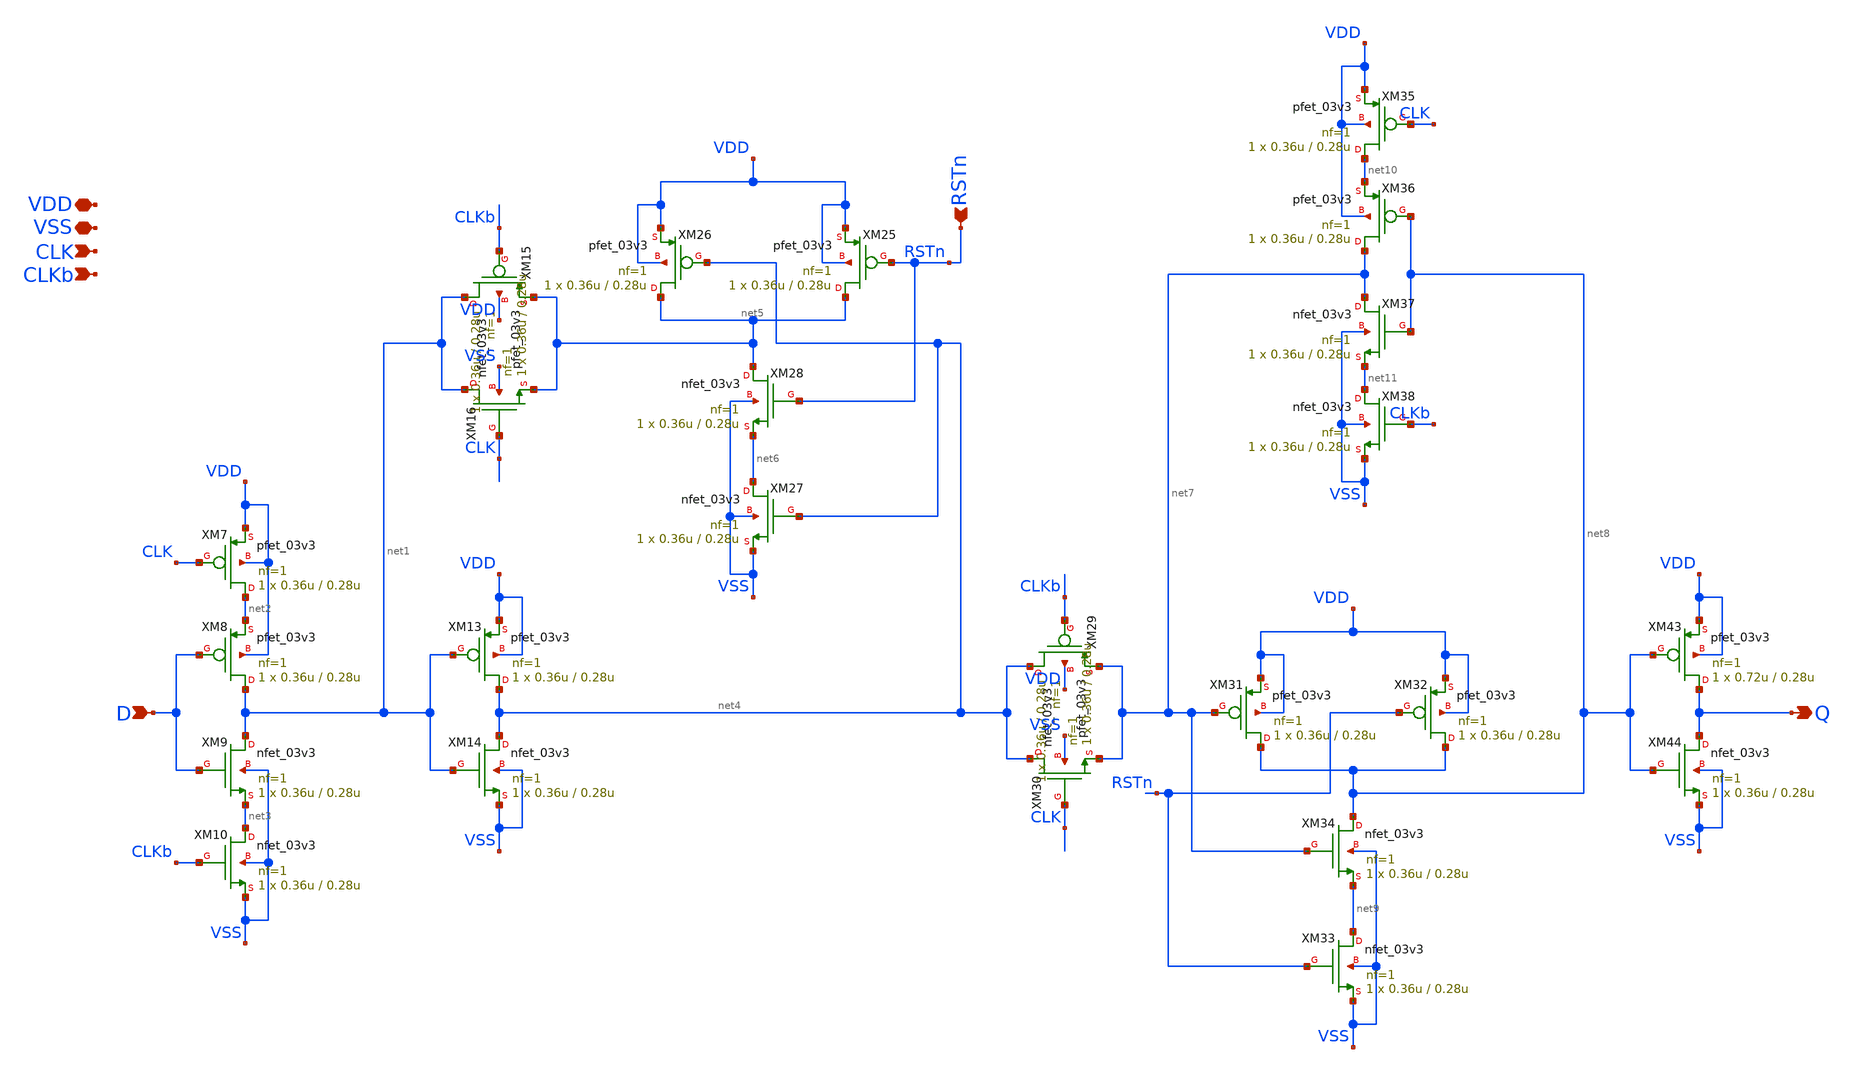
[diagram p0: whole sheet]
** sch_path: CAD6/dff.sch
**.subckt dff D Q RSTn CLK CLKb VDD VSS
*.ipin D
*.opin Q
*.ipin RSTn
*.ipin CLK
*.ipin CLKb
*.iopin VDD
*.iopin VSS
XM7 net2 CLK VDD VDD pfet_03v3 L=0.28u W=0.36u nf=1 ad='int((nf+1)/2) * W/nf * 0.18u' as='int((nf+2)/2) * W/nf * 0.18u'
+ pd='2*int((nf+1)/2) * (W/nf + 0.18u)' ps='2*int((nf+2)/2) * (W/nf + 0.18u)' nrd='0.18u / W' nrs='0.18u / W'
+ sa=0 sb=0 sd=0 m=1
XM8 net1 D net2 VDD pfet_03v3 L=0.28u W=0.36u nf=1 ad='int((nf+1)/2) * W/nf * 0.18u' as='int((nf+2)/2) * W/nf * 0.18u'
+ pd='2*int((nf+1)/2) * (W/nf + 0.18u)' ps='2*int((nf+2)/2) * (W/nf + 0.18u)' nrd='0.18u / W' nrs='0.18u / W'
+ sa=0 sb=0 sd=0 m=1
XM9 net1 D net3 VSS nfet_03v3 L=0.28u W=0.36u nf=1 ad='int((nf+1)/2) * W/nf * 0.18u' as='int((nf+2)/2) * W/nf * 0.18u'
+ pd='2*int((nf+1)/2) * (W/nf + 0.18u)' ps='2*int((nf+2)/2) * (W/nf + 0.18u)' nrd='0.18u / W' nrs='0.18u / W'
+ sa=0 sb=0 sd=0 m=1
XM10 net3 CLKb VSS VSS nfet_03v3 L=0.28u W=0.36u nf=1 ad='int((nf+1)/2) * W/nf * 0.18u' as='int((nf+2)/2) * W/nf * 0.18u'
+ pd='2*int((nf+1)/2) * (W/nf + 0.18u)' ps='2*int((nf+2)/2) * (W/nf + 0.18u)' nrd='0.18u / W' nrs='0.18u / W'
+ sa=0 sb=0 sd=0 m=1
XM13 net4 net1 VDD VDD pfet_03v3 L=0.28u W=0.36u nf=1 ad='int((nf+1)/2) * W/nf * 0.18u' as='int((nf+2)/2) * W/nf * 0.18u'
+ pd='2*int((nf+1)/2) * (W/nf + 0.18u)' ps='2*int((nf+2)/2) * (W/nf + 0.18u)' nrd='0.18u / W' nrs='0.18u / W'
+ sa=0 sb=0 sd=0 m=1
XM14 net4 net1 VSS VSS nfet_03v3 L=0.28u W=0.36u nf=1 ad='int((nf+1)/2) * W/nf * 0.18u' as='int((nf+2)/2) * W/nf * 0.18u'
+ pd='2*int((nf+1)/2) * (W/nf + 0.18u)' ps='2*int((nf+2)/2) * (W/nf + 0.18u)' nrd='0.18u / W' nrs='0.18u / W'
+ sa=0 sb=0 sd=0 m=1
XM15 net1 CLKb net5 VDD pfet_03v3 L=0.28u W=0.36u nf=1 ad='int((nf+1)/2) * W/nf * 0.18u' as='int((nf+2)/2) * W/nf * 0.18u'
+ pd='2*int((nf+1)/2) * (W/nf + 0.18u)' ps='2*int((nf+2)/2) * (W/nf + 0.18u)' nrd='0.18u / W' nrs='0.18u / W'
+ sa=0 sb=0 sd=0 m=1
XM16 net1 CLK net5 VSS nfet_03v3 L=0.28u W=0.36u nf=1 ad='int((nf+1)/2) * W/nf * 0.18u' as='int((nf+2)/2) * W/nf * 0.18u'
+ pd='2*int((nf+1)/2) * (W/nf + 0.18u)' ps='2*int((nf+2)/2) * (W/nf + 0.18u)' nrd='0.18u / W' nrs='0.18u / W'
+ sa=0 sb=0 sd=0 m=1
XM25 net5 RSTn VDD VDD pfet_03v3 L=0.28u W=0.36u nf=1 ad='int((nf+1)/2) * W/nf * 0.18u' as='int((nf+2)/2) * W/nf * 0.18u'
+ pd='2*int((nf+1)/2) * (W/nf + 0.18u)' ps='2*int((nf+2)/2) * (W/nf + 0.18u)' nrd='0.18u / W' nrs='0.18u / W'
+ sa=0 sb=0 sd=0 m=1
XM26 net5 net4 VDD VDD pfet_03v3 L=0.28u W=0.36u nf=1 ad='int((nf+1)/2) * W/nf * 0.18u' as='int((nf+2)/2) * W/nf * 0.18u'
+ pd='2*int((nf+1)/2) * (W/nf + 0.18u)' ps='2*int((nf+2)/2) * (W/nf + 0.18u)' nrd='0.18u / W' nrs='0.18u / W'
+ sa=0 sb=0 sd=0 m=1
XM27 net6 net4 VSS VSS nfet_03v3 L=0.28u W=0.36u nf=1 ad='int((nf+1)/2) * W/nf * 0.18u' as='int((nf+2)/2) * W/nf * 0.18u'
+ pd='2*int((nf+1)/2) * (W/nf + 0.18u)' ps='2*int((nf+2)/2) * (W/nf + 0.18u)' nrd='0.18u / W' nrs='0.18u / W'
+ sa=0 sb=0 sd=0 m=1
XM28 net5 RSTn net6 VSS nfet_03v3 L=0.28u W=0.36u nf=1 ad='int((nf+1)/2) * W/nf * 0.18u' as='int((nf+2)/2) * W/nf * 0.18u'
+ pd='2*int((nf+1)/2) * (W/nf + 0.18u)' ps='2*int((nf+2)/2) * (W/nf + 0.18u)' nrd='0.18u / W' nrs='0.18u / W'
+ sa=0 sb=0 sd=0 m=1
XM29 net4 CLKb net7 VDD pfet_03v3 L=0.28u W=0.36u nf=1 ad='int((nf+1)/2) * W/nf * 0.18u' as='int((nf+2)/2) * W/nf * 0.18u'
+ pd='2*int((nf+1)/2) * (W/nf + 0.18u)' ps='2*int((nf+2)/2) * (W/nf + 0.18u)' nrd='0.18u / W' nrs='0.18u / W'
+ sa=0 sb=0 sd=0 m=1
XM30 net4 CLK net7 VSS nfet_03v3 L=0.28u W=0.36u nf=1 ad='int((nf+1)/2) * W/nf * 0.18u' as='int((nf+2)/2) * W/nf * 0.18u'
+ pd='2*int((nf+1)/2) * (W/nf + 0.18u)' ps='2*int((nf+2)/2) * (W/nf + 0.18u)' nrd='0.18u / W' nrs='0.18u / W'
+ sa=0 sb=0 sd=0 m=1
XM31 net8 net7 VDD VDD pfet_03v3 L=0.28u W=0.36u nf=1 ad='int((nf+1)/2) * W/nf * 0.18u' as='int((nf+2)/2) * W/nf * 0.18u'
+ pd='2*int((nf+1)/2) * (W/nf + 0.18u)' ps='2*int((nf+2)/2) * (W/nf + 0.18u)' nrd='0.18u / W' nrs='0.18u / W'
+ sa=0 sb=0 sd=0 m=1
XM32 net8 RSTn VDD VDD pfet_03v3 L=0.28u W=0.36u nf=1 ad='int((nf+1)/2) * W/nf * 0.18u' as='int((nf+2)/2) * W/nf * 0.18u'
+ pd='2*int((nf+1)/2) * (W/nf + 0.18u)' ps='2*int((nf+2)/2) * (W/nf + 0.18u)' nrd='0.18u / W' nrs='0.18u / W'
+ sa=0 sb=0 sd=0 m=1
XM33 net9 RSTn VSS VSS nfet_03v3 L=0.28u W=0.36u nf=1 ad='int((nf+1)/2) * W/nf * 0.18u' as='int((nf+2)/2) * W/nf * 0.18u'
+ pd='2*int((nf+1)/2) * (W/nf + 0.18u)' ps='2*int((nf+2)/2) * (W/nf + 0.18u)' nrd='0.18u / W' nrs='0.18u / W'
+ sa=0 sb=0 sd=0 m=1
XM34 net8 net7 net9 VSS nfet_03v3 L=0.28u W=0.36u nf=1 ad='int((nf+1)/2) * W/nf * 0.18u' as='int((nf+2)/2) * W/nf * 0.18u'
+ pd='2*int((nf+1)/2) * (W/nf + 0.18u)' ps='2*int((nf+2)/2) * (W/nf + 0.18u)' nrd='0.18u / W' nrs='0.18u / W'
+ sa=0 sb=0 sd=0 m=1
XM35 net10 CLK VDD VDD pfet_03v3 L=0.28u W=0.36u nf=1 ad='int((nf+1)/2) * W/nf * 0.18u' as='int((nf+2)/2) * W/nf * 0.18u'
+ pd='2*int((nf+1)/2) * (W/nf + 0.18u)' ps='2*int((nf+2)/2) * (W/nf + 0.18u)' nrd='0.18u / W' nrs='0.18u / W'
+ sa=0 sb=0 sd=0 m=1
XM36 net7 net8 net10 VDD pfet_03v3 L=0.28u W=0.36u nf=1 ad='int((nf+1)/2) * W/nf * 0.18u' as='int((nf+2)/2) * W/nf * 0.18u'
+ pd='2*int((nf+1)/2) * (W/nf + 0.18u)' ps='2*int((nf+2)/2) * (W/nf + 0.18u)' nrd='0.18u / W' nrs='0.18u / W'
+ sa=0 sb=0 sd=0 m=1
XM37 net7 net8 net11 VSS nfet_03v3 L=0.28u W=0.36u nf=1 ad='int((nf+1)/2) * W/nf * 0.18u' as='int((nf+2)/2) * W/nf * 0.18u'
+ pd='2*int((nf+1)/2) * (W/nf + 0.18u)' ps='2*int((nf+2)/2) * (W/nf + 0.18u)' nrd='0.18u / W' nrs='0.18u / W'
+ sa=0 sb=0 sd=0 m=1
XM38 net11 CLKb VSS VSS nfet_03v3 L=0.28u W=0.36u nf=1 ad='int((nf+1)/2) * W/nf * 0.18u' as='int((nf+2)/2) * W/nf * 0.18u'
+ pd='2*int((nf+1)/2) * (W/nf + 0.18u)' ps='2*int((nf+2)/2) * (W/nf + 0.18u)' nrd='0.18u / W' nrs='0.18u / W'
+ sa=0 sb=0 sd=0 m=1
XM43 Q net8 VDD VDD pfet_03v3 L=0.28u W=0.72u nf=1 ad='int((nf+1)/2) * W/nf * 0.18u' as='int((nf+2)/2) * W/nf * 0.18u'
+ pd='2*int((nf+1)/2) * (W/nf + 0.18u)' ps='2*int((nf+2)/2) * (W/nf + 0.18u)' nrd='0.18u / W' nrs='0.18u / W'
+ sa=0 sb=0 sd=0 m=1
XM44 Q net8 VSS VSS nfet_03v3 L=0.28u W=0.36u nf=1 ad='int((nf+1)/2) * W/nf * 0.18u' as='int((nf+2)/2) * W/nf * 0.18u'
+ pd='2*int((nf+1)/2) * (W/nf + 0.18u)' ps='2*int((nf+2)/2) * (W/nf + 0.18u)' nrd='0.18u / W' nrs='0.18u / W'
+ sa=0 sb=0 sd=0 m=1
**.ends
.end
